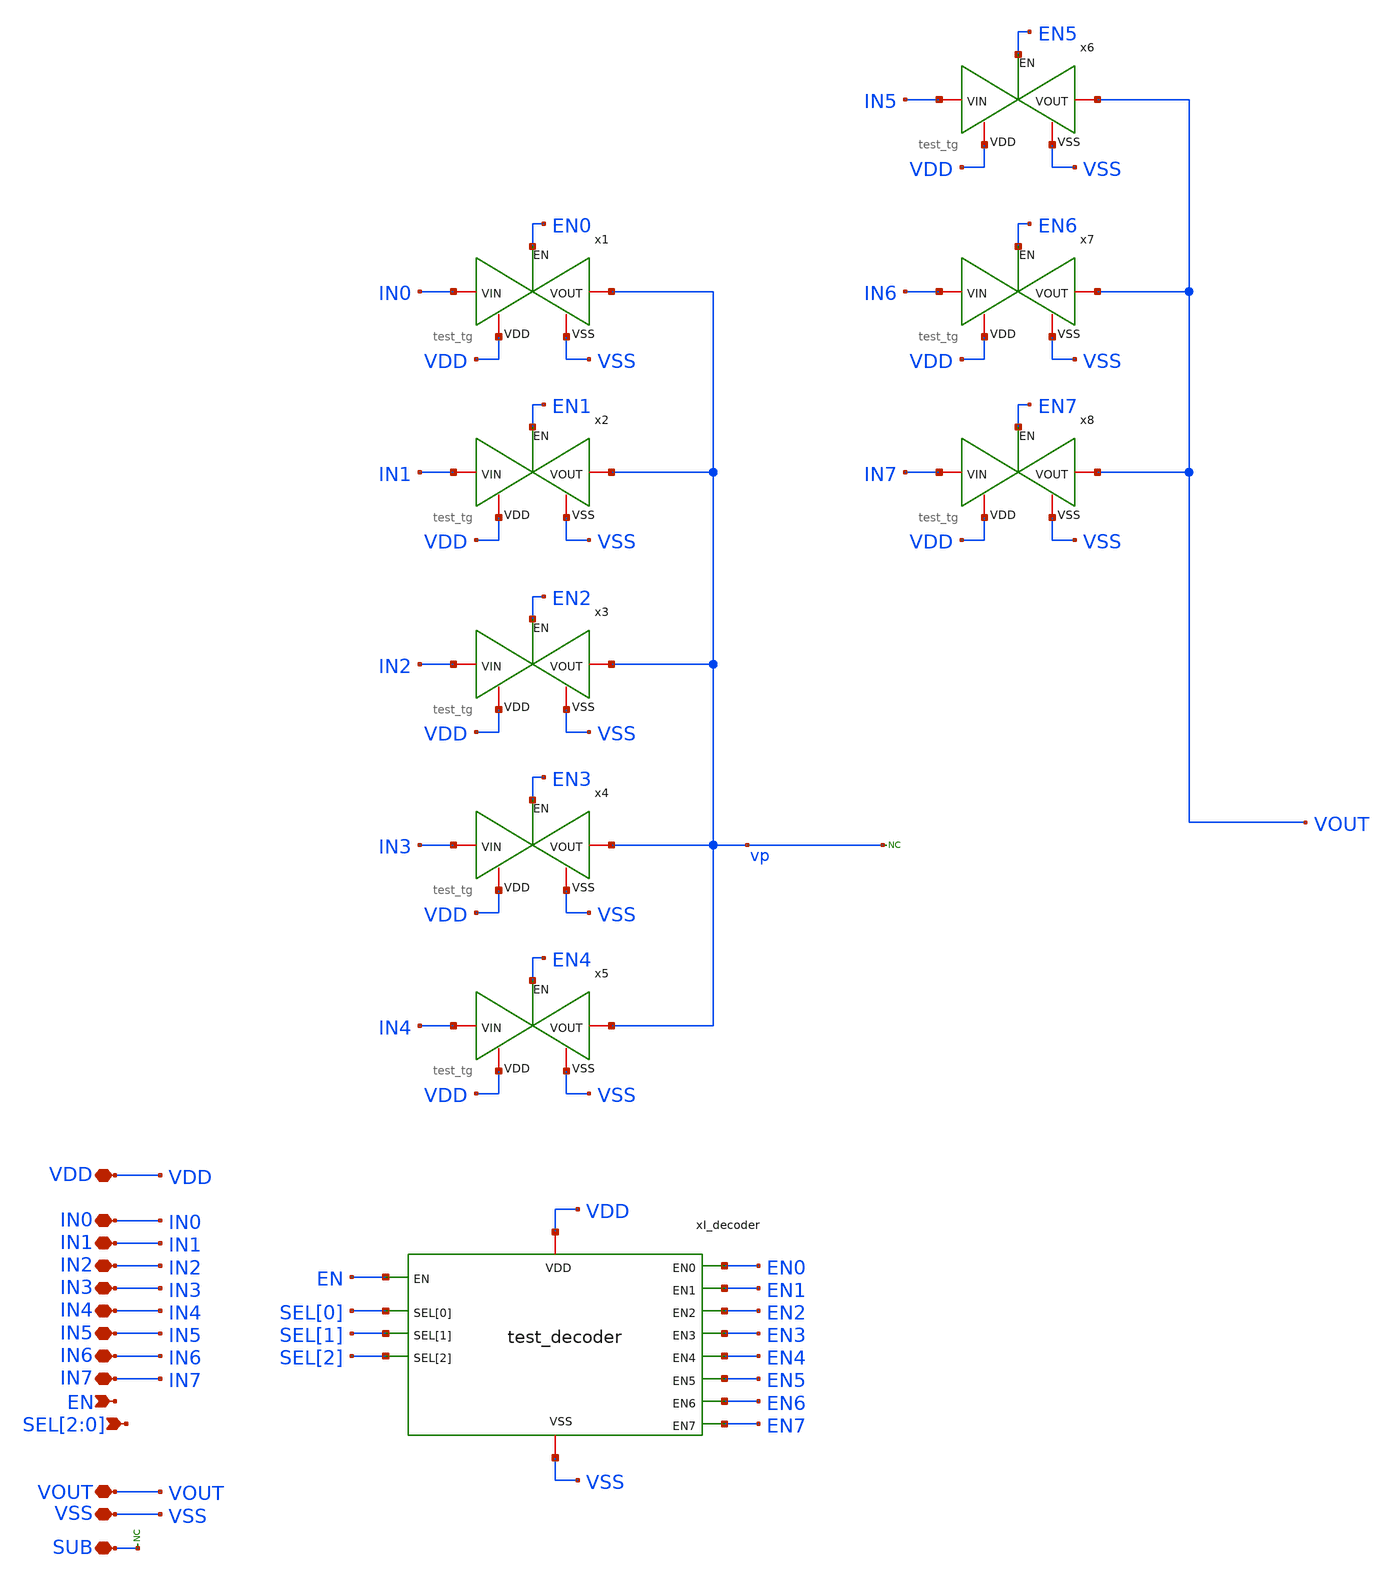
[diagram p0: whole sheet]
** sch_path: designs/libs/core_test/test/test_v2.sch
**.subckt test_v2 VDD VSS SUB VOUT EN SEL[2],SEL[1],SEL[0] IN0 IN1 IN2 IN3 IN4 IN5 IN6 IN7
*.iopin VDD
*.iopin VSS
*.iopin SUB
*.iopin VOUT
*.ipin EN
*.ipin SEL[2],SEL[1],SEL[0]
*.iopin IN0
*.iopin IN1
*.iopin IN2
*.iopin IN3
*.iopin IN4
*.iopin IN5
*.iopin IN6
*.iopin IN7
* noconn SUB
x1 VDD EN0 IN0 vp VSS test_tg
x2 VDD EN1 IN1 vp VSS test_tg
x3 VDD EN2 IN2 vp VSS test_tg
x4 VDD EN3 IN3 vp VSS test_tg
x5 VDD EN4 IN4 vp VSS test_tg
x6 VDD EN5 IN5 VOUT VSS test_tg
x7 VDD EN6 IN6 VOUT VSS test_tg
x8 VDD EN7 IN7 VOUT VSS test_tg
xI_decoder SEL[0] SEL[1] SEL[2] VDD VSS EN0 EN1 EN2 EN3 EN4 EN5 EN6 EN7 EN test_decoder
* noconn vp
**.ends

* expanding   symbol:  libs/core_test/test_tg/test_tg.sym # of pins=5
** sym_path: designs/libs/core_test/test_tg/test_tg.sym
** sch_path: designs/libs/core_test/test_tg/test_tg.sch
.subckt test_tg VDD EN VIN VOUT VSS
*.iopin VIN
*.iopin VOUT
*.ipin EN
*.iopin VDD
*.iopin VSS
XM1 VIN EN VOUT VSS nfet_05v0 L=0.60u W=1.5u nf=1 ad='int((nf+1)/2) * W/nf * 0.18u' as='int((nf+2)/2) * W/nf * 0.18u'
+ pd='2*int((nf+1)/2) * (W/nf + 0.18u)' ps='2*int((nf+2)/2) * (W/nf + 0.18u)' nrd='0.18u / W' nrs='0.18u / W'
+ sa=0 sb=0 sd=0 m=2
XM2 VOUT ENB VIN VDD pfet_05v0 L=0.50u W=1.5u nf=1 ad='int((nf+1)/2) * W/nf * 0.18u' as='int((nf+2)/2) * W/nf * 0.18u'
+ pd='2*int((nf+1)/2) * (W/nf + 0.18u)' ps='2*int((nf+2)/2) * (W/nf + 0.18u)' nrd='0.18u / W' nrs='0.18u / W'
+ sa=0 sb=0 sd=0 m=6
x1 VDD ENB EN VSS test_inv
.ends


* expanding   symbol:  libs/core_test/test_decoder/test_decoder.sym # of pins=14
** sym_path: designs/libs/core_test/test_decoder/test_decoder.sym
** sch_path: designs/libs/core_test/test_decoder/test_decoder.sch
.subckt test_decoder SEL[0] SEL[1] SEL[2] VDD VSS EN0 EN1 EN2 EN3 EN4 EN5 EN6 EN7 EN
*.iopin VDD
*.iopin VSS
*.ipin SEL[0]
*.ipin SEL[1]
*.ipin SEL[2]
*.opin EN0
*.opin EN1
*.opin EN2
*.opin EN3
*.opin EN4
*.opin EN5
*.opin EN6
*.opin EN7
*.ipin EN
x3 VDD SEL[0] net1 SEL[1] VSS test_and
x4 VDD net1 net2 SEL[2] VSS test_and
x5 VDD EN0_in net2 VSS test_inv
x6 VDD SEL[0] net3 SEL[1] VSS test_and
x7 VDD net4 net3 VSS test_inv
x8 VDD net4 EN1_in SEL[2] VSS test_and
x9 VDD net5 SEL[0] VSS test_inv
x10 VDD net5 net7 SEL[1] VSS test_and
x11 VDD net6 SEL[2] VSS test_inv
x12 VDD net7 EN2_in net6 VSS test_and
x13 VDD net8 SEL[0] VSS test_inv
x14 VDD net8 net9 SEL[1] VSS test_and
x15 VDD net9 EN3_in SEL[2] VSS test_and
x16 VDD SEL[1] net10 SEL[2] VSS test_and
x17 VDD net11 net10 VSS test_inv
x18 VDD SEL[0] EN4_in net11 VSS test_and
x19 VDD net12 SEL[1] VSS test_inv
x20 VDD SEL[0] net13 net12 VSS test_and
x21 VDD net13 EN5_in SEL[2] VSS test_and
x22 VDD SEL[0] net14 SEL[1] VSS test_and
x23 VDD net14 EN6_in net15 VSS test_and
x24 VDD net15 SEL[2] VSS test_inv
x25 VDD SEL[0] net16 SEL[1] VSS test_and
x26 VDD net16 EN7_in SEL[2] VSS test_and
x1 VDD EN0_in EN0 EN VSS test_and
x2 VDD EN1_in EN1 EN VSS test_and
x27 VDD EN2_in EN2 EN VSS test_and
x28 VDD EN3_in EN3 EN VSS test_and
x29 VDD EN4_in EN4 EN VSS test_and
x30 VDD EN5_in EN5 EN VSS test_and
x31 VDD EN6_in EN6 EN VSS test_and
x32 VDD EN7_in EN7 EN VSS test_and
.ends


* expanding   symbol:  libs/core_test/test_inv/test_inv.sym # of pins=4
** sym_path: designs/libs/core_test/test_inv/test_inv.sym
** sch_path: designs/libs/core_test/test_inv/test_inv.sch
.subckt test_inv VDD OUT IN VSS
*.opin OUT
*.ipin IN
*.iopin VDD
*.iopin VSS
XM1 OUT IN VSS VSS nfet_05v0 L=0.60u W=0.30u nf=1 ad='int((nf+1)/2) * W/nf * 0.18u' as='int((nf+2)/2) * W/nf * 0.18u'
+ pd='2*int((nf+1)/2) * (W/nf + 0.18u)' ps='2*int((nf+2)/2) * (W/nf + 0.18u)' nrd='0.18u / W' nrs='0.18u / W'
+ sa=0 sb=0 sd=0 m=1
XM2 OUT IN VDD VDD pfet_05v0 L=0.50u W=0.30u nf=2 ad='int((nf+1)/2) * W/nf * 0.18u' as='int((nf+2)/2) * W/nf * 0.18u'
+ pd='2*int((nf+1)/2) * (W/nf + 0.18u)' ps='2*int((nf+2)/2) * (W/nf + 0.18u)' nrd='0.18u / W' nrs='0.18u / W'
+ sa=0 sb=0 sd=0 m=1
.ends


* expanding   symbol:  libs/core_test/test_and/test_and.sym # of pins=5
** sym_path: designs/libs/core_test/test_and/test_and.sym
** sch_path: designs/libs/core_test/test_and/test_and.sch
.subckt test_and VDD A Y B VSS
*.ipin A
*.ipin B
*.iopin VDD
*.iopin VSS
*.opin Y
XM1 net1 A net2 VSS nfet_05v0 L=0.60u W=0.50u nf=1 ad='int((nf+1)/2) * W/nf * 0.18u' as='int((nf+2)/2) * W/nf * 0.18u'
+ pd='2*int((nf+1)/2) * (W/nf + 0.18u)' ps='2*int((nf+2)/2) * (W/nf + 0.18u)' nrd='0.18u / W' nrs='0.18u / W'
+ sa=0 sb=0 sd=0 m=1
XM2 net1 A VDD VDD pfet_05v0 L=0.50u W=0.50u nf=1 ad='int((nf+1)/2) * W/nf * 0.18u' as='int((nf+2)/2) * W/nf * 0.18u'
+ pd='2*int((nf+1)/2) * (W/nf + 0.18u)' ps='2*int((nf+2)/2) * (W/nf + 0.18u)' nrd='0.18u / W' nrs='0.18u / W'
+ sa=0 sb=0 sd=0 m=1
XM3 net1 B VDD VDD pfet_05v0 L=0.50u W=0.50u nf=1 ad='int((nf+1)/2) * W/nf * 0.18u' as='int((nf+2)/2) * W/nf * 0.18u'
+ pd='2*int((nf+1)/2) * (W/nf + 0.18u)' ps='2*int((nf+2)/2) * (W/nf + 0.18u)' nrd='0.18u / W' nrs='0.18u / W'
+ sa=0 sb=0 sd=0 m=1
XM4 net2 B VSS VSS nfet_05v0 L=0.60u W=0.50u nf=1 ad='int((nf+1)/2) * W/nf * 0.18u' as='int((nf+2)/2) * W/nf * 0.18u'
+ pd='2*int((nf+1)/2) * (W/nf + 0.18u)' ps='2*int((nf+2)/2) * (W/nf + 0.18u)' nrd='0.18u / W' nrs='0.18u / W'
+ sa=0 sb=0 sd=0 m=1
XM5 Y net1 VSS VSS nfet_05v0 L=0.60u W=0.50u nf=1 ad='int((nf+1)/2) * W/nf * 0.18u' as='int((nf+2)/2) * W/nf * 0.18u'
+ pd='2*int((nf+1)/2) * (W/nf + 0.18u)' ps='2*int((nf+2)/2) * (W/nf + 0.18u)' nrd='0.18u / W' nrs='0.18u / W'
+ sa=0 sb=0 sd=0 m=1
XM6 Y net1 VDD VDD pfet_05v0 L=0.50u W=0.50u nf=1 ad='int((nf+1)/2) * W/nf * 0.18u' as='int((nf+2)/2) * W/nf * 0.18u'
+ pd='2*int((nf+1)/2) * (W/nf + 0.18u)' ps='2*int((nf+2)/2) * (W/nf + 0.18u)' nrd='0.18u / W' nrs='0.18u / W'
+ sa=0 sb=0 sd=0 m=1
.ends

.end
